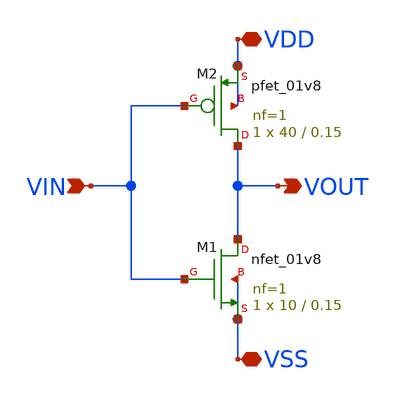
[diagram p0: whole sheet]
** sch_path: xschem/DC_DC_Converter_xschem/OTHERS/DC_DC_Converter_JV10/DELAY_JAWAD/Inverter_D2.sch
**.subckt Inverter_D2 VIN VDD VSS VOUT
*.ipin VIN
*.iopin VDD
*.iopin VSS
*.opin VOUT
XM1 VOUT VIN VSS VSS sky130_fd_pr__nfet_01v8 L=0.15 W=10 nf=1 ad='int((nf+1)/2) * W/nf * 0.29' as='int((nf+2)/2) * W/nf * 0.29'
+ pd='2*int((nf+1)/2) * (W/nf + 0.29)' ps='2*int((nf+2)/2) * (W/nf + 0.29)' nrd='0.29 / W' nrs='0.29 / W'
+ sa=0 sb=0 sd=0 mult=1 m=1
XM2 VOUT VIN VDD VDD sky130_fd_pr__pfet_01v8 L=0.15 W=40 nf=1 ad='int((nf+1)/2) * W/nf * 0.29' as='int((nf+2)/2) * W/nf * 0.29'
+ pd='2*int((nf+1)/2) * (W/nf + 0.29)' ps='2*int((nf+2)/2) * (W/nf + 0.29)' nrd='0.29 / W' nrs='0.29 / W'
+ sa=0 sb=0 sd=0 mult=1 m=1
**.ends
.end
